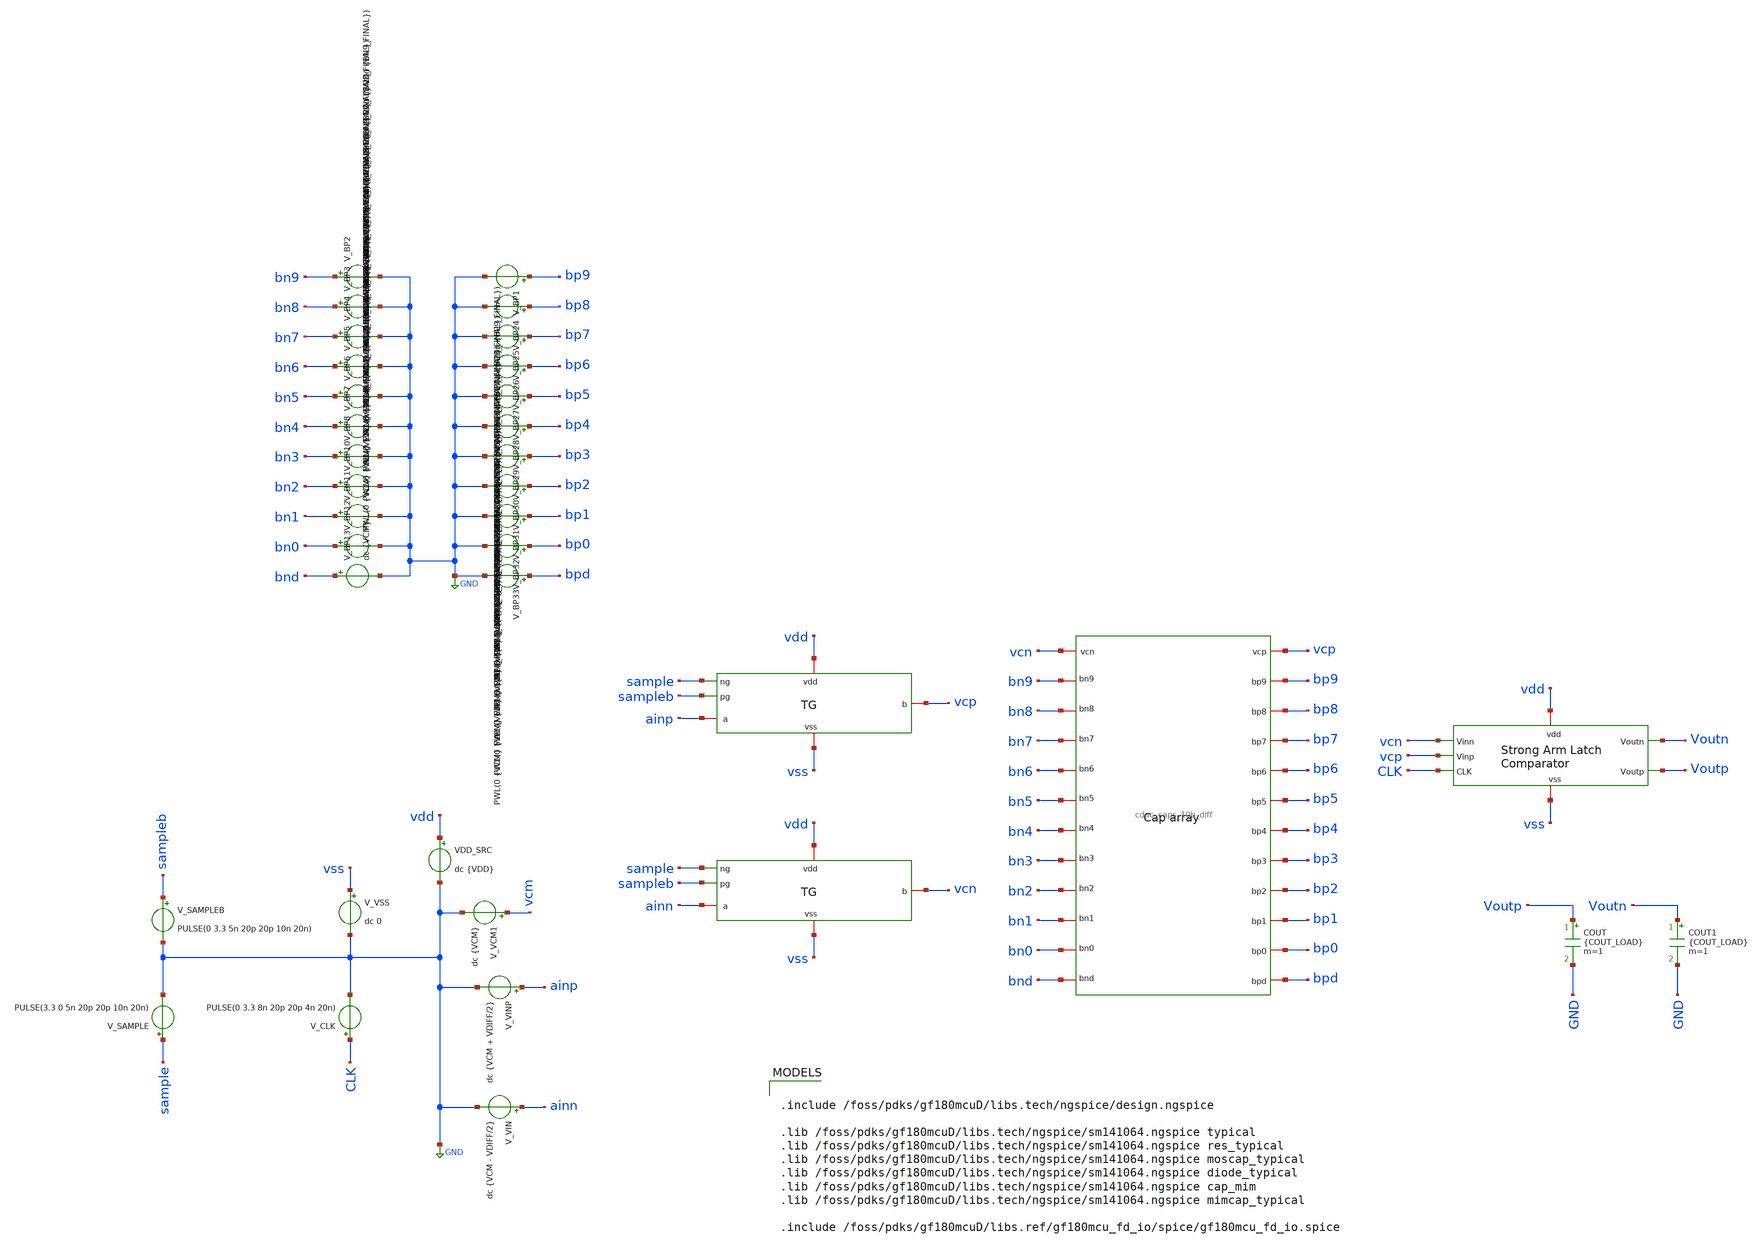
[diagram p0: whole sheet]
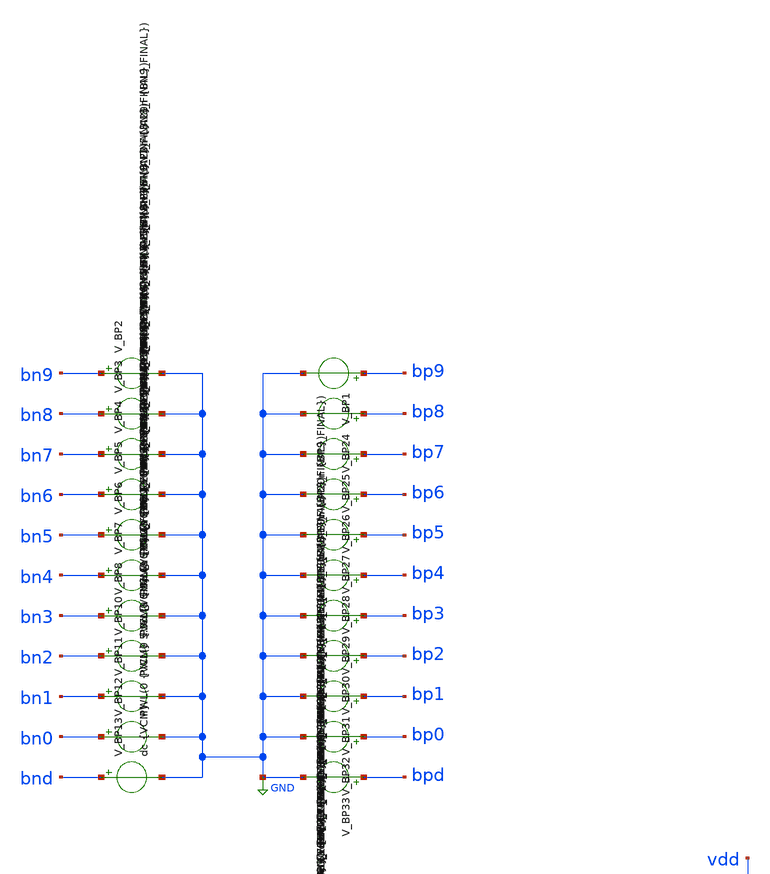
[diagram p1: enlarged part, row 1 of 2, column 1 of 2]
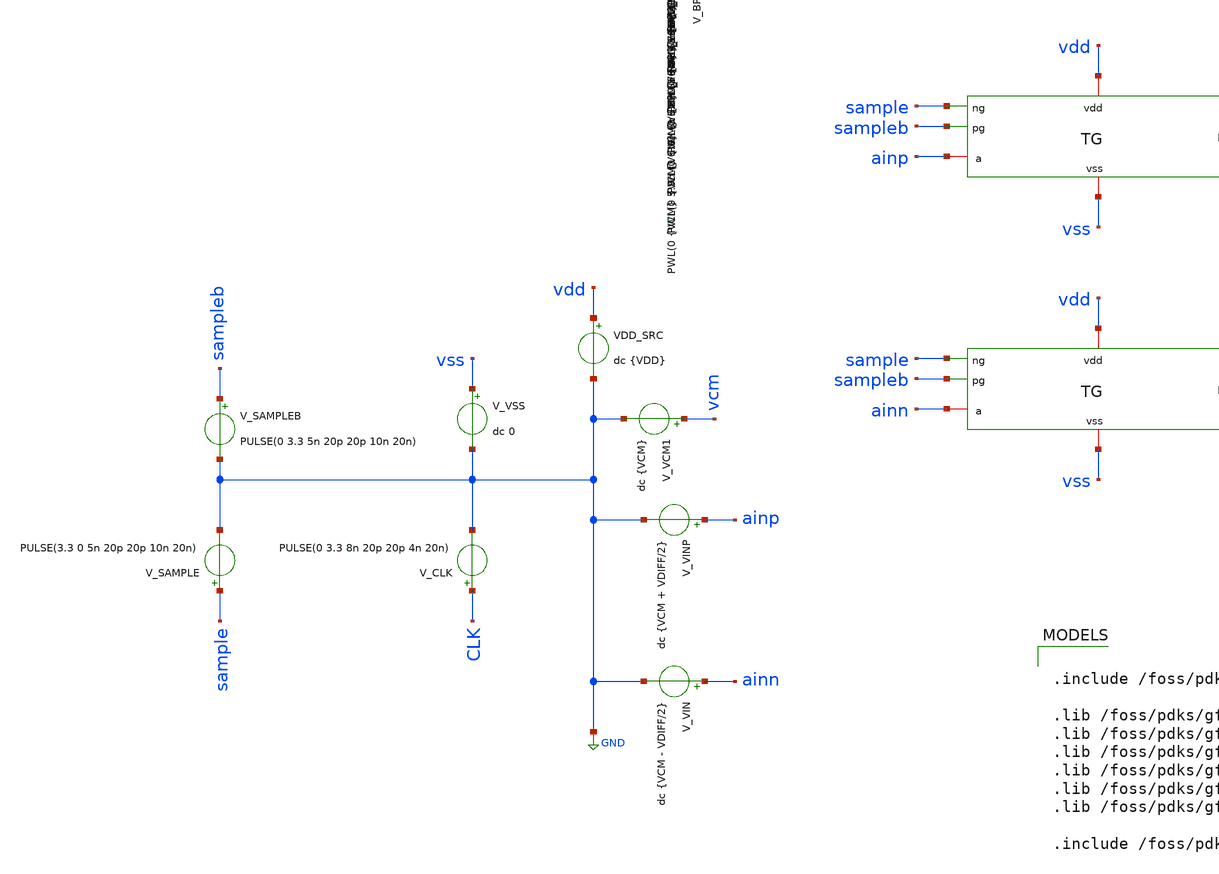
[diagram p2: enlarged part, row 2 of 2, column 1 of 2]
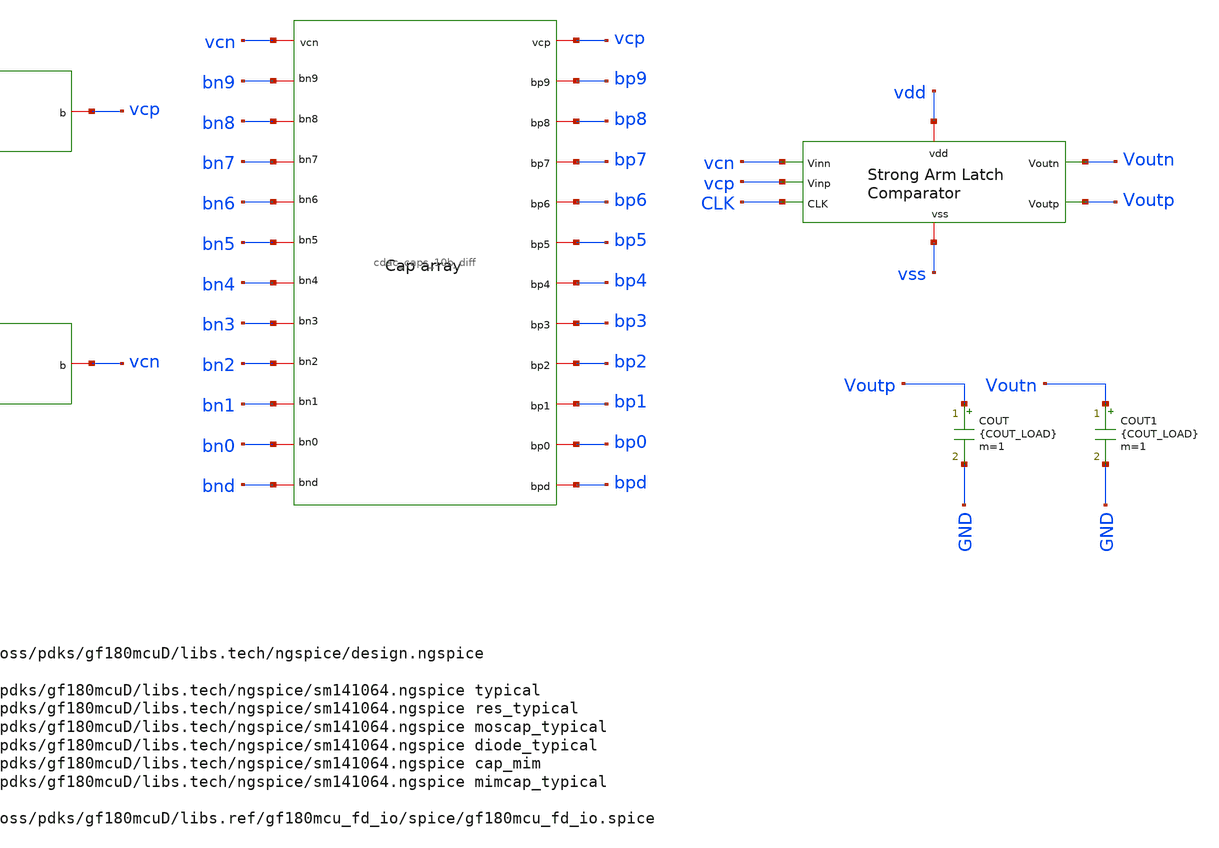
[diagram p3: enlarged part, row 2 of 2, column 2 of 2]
** sch_path: circuit_files/sar_adc_test/tb/cdac_comp_msb_step_tb.sch
**.subckt cdac_comp_msb_step_tb
V_VIN ainn GND dc {VCM - VDIFF/2}
VDD_SRC vdd GND dc {VDD}
V_VINP ainp GND dc {VCM + VDIFF/2}
V_VSS vss GND dc 0
V_CLK CLK GND PULSE(0 3.3 8n 20p 20p 4n 20n)
COUT Voutp GND {COUT_LOAD} m=1
COUT1 Voutn GND {COUT_LOAD} m=1
x1 Voutn vcn Voutp vcp vdd vss CLK strong_arm_comp
x3 vss sample sampleb vdd ainp vcp tg
x4 vss sample sampleb vdd ainn vcn tg
V_SAMPLE sample GND PULSE(3.3 0 5n 20p 20p 10n 20n)
V_SAMPLEB sampleb GND PULSE(0 3.3 5n 20p 20p 10n 20n)
V_VCM1 vcm GND dc {VCM}
x2 vcp bp3 bp0 bp5 bp2 bpd bp1 bp7 bp6 bp8 bp4 bp9 vcn bn0 bn1 bn8 bn7 bn6 bn5 bn4 bn3 bn9 bn2 bnd
+ cdac_caps_10b_diff
V_BP1 bp9 GND PWL(0 {VCM} 5.9n {VCM} 6n {BP9_FINAL} 20n {BP9_FINAL})
V_BP24 bp8 GND PWL(0 {VCM} 5.9n {VCM} 6n {BP8_FINAL} 20n {BP8_FINAL})
V_BP25 bp7 GND PWL(0 {VCM} 5.9n {VCM} 6n {BP7_FINAL} 20n {BP7_FINAL})
V_BP26 bp6 GND PWL(0 {VCM} 5.9n {VCM} 6n {BP6_FINAL} 20n {BP6_FINAL})
V_BP27 bp5 GND PWL(0 {VCM} 5.9n {VCM} 6n {BP5_FINAL} 20n {BP5_FINAL})
V_BP28 bp4 GND PWL(0 {VCM} 5.9n {VCM} 6n {BP4_FINAL} 20n {BP4_FINAL})
V_BP29 bp3 GND PWL(0 {VCM} 5.9n {VCM} 6n {BP3_FINAL} 20n {BP3_FINAL})
V_BP30 bp2 GND PWL(0 {VCM} 5.9n {VCM} 6n {BP2_FINAL} 20n {BP2_FINAL})
V_BP31 bp1 GND PWL(0 {VCM} 5.9n {VCM} 6n {BP1_FINAL} 20n {BP1_FINAL})
V_BP32 bp0 GND PWL(0 {VCM} 5.9n {VCM} 6n {BP0_FINAL} 20n {BP0_FINAL})
V_BP33 bpd GND dc {VCM}
V_BP2 bn9 GND PWL(0 {VCM} 5.9n {VCM} 6n {BN9_FINAL} 20n {BN9_FINAL})
V_BP3 bn8 GND PWL(0 {VCM} 5.9n {VCM} 6n {BN8_FINAL} 20n {BN8_FINAL})
V_BP4 bn7 GND PWL(0 {VCM} 5.9n {VCM} 6n {BN7_FINAL} 20n {BN7_FINAL})
V_BP5 bn6 GND PWL(0 {VCM} 5.9n {VCM} 6n {BN6_FINAL} 20n {BN6_FINAL})
V_BP6 bn5 GND PWL(0 {VCM} 5.9n {VCM} 6n {BN5_FINAL} 20n {BN5_FINAL})
V_BP7 bn4 GND PWL(0 {VCM} 5.9n {VCM} 6n {BN4_FINAL} 20n {BN4_FINAL})
V_BP8 bn3 GND PWL(0 {VCM} 5.9n {VCM} 6n {BN3_FINAL} 20n {BN3_FINAL})
V_BP10 bn2 GND PWL(0 {VCM} 5.9n {VCM} 6n {BN2_FINAL} 20n {BN2_FINAL})
V_BP11 bn1 GND PWL(0 {VCM} 5.9n {VCM} 6n {BN1_FINAL} 20n {BN1_FINAL})
V_BP12 bn0 GND PWL(0 {VCM} 5.9n {VCM} 6n {BN0_FINAL} 20n {BN0_FINAL})
V_BP13 bnd GND dc {VCM}
**** begin user architecture code

.include /foss/pdks/gf180mcuD/libs.tech/ngspice/design.ngspice

.lib /foss/pdks/gf180mcuD/libs.tech/ngspice/sm141064.ngspice typical
.lib /foss/pdks/gf180mcuD/libs.tech/ngspice/sm141064.ngspice res_typical
.lib /foss/pdks/gf180mcuD/libs.tech/ngspice/sm141064.ngspice moscap_typical
.lib /foss/pdks/gf180mcuD/libs.tech/ngspice/sm141064.ngspice diode_typical
.lib /foss/pdks/gf180mcuD/libs.tech/ngspice/sm141064.ngspice cap_mim
.lib /foss/pdks/gf180mcuD/libs.tech/ngspice/sm141064.ngspice mimcap_typical

.include /foss/pdks/gf180mcuD/libs.ref/gf180mcu_fd_io/spice/gf180mcu_fd_io.spice



.param VDD=3.3
.param VCM=1.65
.param VDIFF=0
.param WCU=5u
.param LCU=5u
.param COUT_LOAD=20f

* Positive MSB test:
* bp9 goes high, bn9 goes low.
.param BP9_FINAL={VDD}
.param BN9_FINAL=0

* All other bits stay at VCM.
.param BP8_FINAL={VCM}
.param BP7_FINAL={VCM}
.param BP6_FINAL={VCM}
.param BP5_FINAL={VCM}
.param BP4_FINAL={VCM}
.param BP3_FINAL={VCM}
.param BP2_FINAL={VCM}
.param BP1_FINAL={VCM}
.param BP0_FINAL={VCM}

.param BN8_FINAL={VCM}
.param BN7_FINAL={VCM}
.param BN6_FINAL={VCM}
.param BN5_FINAL={VCM}
.param BN4_FINAL={VCM}
.param BN3_FINAL={VCM}
.param BN2_FINAL={VCM}
.param BN1_FINAL={VCM}
.param BN0_FINAL={VCM}


.options savecurrents
.options reltol=1e-4 abstol=1e-12 vntol=1e-6 method=gear

.save v(sample) v(sampleb) v(CLK)
.save v(ainp) v(ainn)
.save v(vcp) v(vcn)
.save v(bp9) v(bn9)
.save v(Voutp) v(Voutn)
.save i(VDD_SRC)

.control

shell rm -f cdac_bit_weight_sweep_results.txt

echo ================================================== > cdac_bit_weight_sweep_results.txt
echo CDAC BIT-WEIGHT SWEEP RESULTS >> cdac_bit_weight_sweep_results.txt
echo ================================================== >> cdac_bit_weight_sweep_results.txt
echo Sweep type: positive differential CDAC steps >> cdac_bit_weight_sweep_results.txt
echo For each bit k: bp[k] switches VCM to VDD, bn[k] switches VCM to 0 >>
+ cdac_bit_weight_sweep_results.txt
echo All other bottom plates stay at VCM >> cdac_bit_weight_sweep_results.txt
echo Dummy caps bpd and bnd stay at VCM >> cdac_bit_weight_sweep_results.txt
echo VDD = 3.3 V >> cdac_bit_weight_sweep_results.txt
echo VCM = 1.65 V >> cdac_bit_weight_sweep_results.txt
echo Unit cap uses cap_mim_2f0fF with WCU=5um and LCU=5um >> cdac_bit_weight_sweep_results.txt
echo Approx Cu = 2 fF/um2 * 5um * 5um = 50 fF >> cdac_bit_weight_sweep_results.txt
echo Approx total capacitance per side = 1024*50fF = 51.2 pF >> cdac_bit_weight_sweep_results.txt
echo Sample turns OFF at 5 ns >> cdac_bit_weight_sweep_results.txt
echo CDAC bottom plates switch at 6 ns >> cdac_bit_weight_sweep_results.txt
echo CDAC step measured at 7 ns >> cdac_bit_weight_sweep_results.txt
echo Comparator CLK rises at 8 ns >> cdac_bit_weight_sweep_results.txt
echo Comparator output measured at 10 ns >> cdac_bit_weight_sweep_results.txt
echo pass_weight = 1 if CDAC step error is less than 10 percent >> cdac_bit_weight_sweep_results.txt
echo pass_comp = 1 if comparator output has correct positive polarity >>
+ cdac_bit_weight_sweep_results.txt
echo ================================================== >> cdac_bit_weight_sweep_results.txt
echo columns: BIT expected_step measured_step abs_error rel_error_percent vdiff_before vdiff_after
+ vcp_5p5 vcn_5p5 vcp_7 vcn_7 cm_7 voutp_10 voutn_10 outdiff_10 pass_weight pass_comp iavg_0_10ns pavg_0_10ns
+ >> cdac_bit_weight_sweep_results.txt
echo ================================================== >> cdac_bit_weight_sweep_results.txt


* ==================================================
* BIT 9 POSITIVE STEP
* ==================================================
alterparam BP9_FINAL = 3.3
alterparam BP8_FINAL = 1.65
alterparam BP7_FINAL = 1.65
alterparam BP6_FINAL = 1.65
alterparam BP5_FINAL = 1.65
alterparam BP4_FINAL = 1.65
alterparam BP3_FINAL = 1.65
alterparam BP2_FINAL = 1.65
alterparam BP1_FINAL = 1.65
alterparam BP0_FINAL = 1.65

alterparam BN9_FINAL = 0
alterparam BN8_FINAL = 1.65
alterparam BN7_FINAL = 1.65
alterparam BN6_FINAL = 1.65
alterparam BN5_FINAL = 1.65
alterparam BN4_FINAL = 1.65
alterparam BN3_FINAL = 1.65
alterparam BN2_FINAL = 1.65
alterparam BN1_FINAL = 1.65
alterparam BN0_FINAL = 1.65

reset
tran 1p 12n

meas tran vcp55 FIND v(vcp) AT=5.5n
meas tran vcn55 FIND v(vcn) AT=5.5n
let vdiff_before = vcp55 - vcn55

meas tran vcp7 FIND v(vcp) AT=7n
meas tran vcn7 FIND v(vcn) AT=7n
let vdiff_after = vcp7 - vcn7
let measured_step = vdiff_after - vdiff_before
let expected_step = 1.65
let abs_error = abs(measured_step - expected_step)
let rel_error_percent = 100*abs_error/expected_step
let cm7 = 0.5*(vcp7 + vcn7)

meas tran voutp10 FIND v(Voutp) AT=10n
meas tran voutn10 FIND v(Voutn) AT=10n
let outdiff10 = voutp10 - voutn10

let pass_weight = 0
if rel_error_percent < 10
  let pass_weight = 1
end

let pass_comp = 0
if outdiff10 > 2.5
  let pass_comp = 1
end

meas tran iavg AVG i(VDD_SRC) FROM=0n TO=10n
let pavg = abs(3.3*iavg)

echo 9 $&expected_step $&measured_step $&abs_error $&rel_error_percent $&vdiff_before $&vdiff_after
+ $&vcp55 $&vcn55 $&vcp7 $&vcn7 $&cm7 $&voutp10 $&voutn10 $&outdiff10 $&pass_weight $&pass_comp $&iavg $&pavg
+ >> cdac_bit_weight_sweep_results.txt


* ==================================================
* BIT 8 POSITIVE STEP
* ==================================================
alterparam BP9_FINAL = 1.65
alterparam BP8_FINAL = 3.3
alterparam BP7_FINAL = 1.65
alterparam BP6_FINAL = 1.65
alterparam BP5_FINAL = 1.65
alterparam BP4_FINAL = 1.65
alterparam BP3_FINAL = 1.65
alterparam BP2_FINAL = 1.65
alterparam BP1_FINAL = 1.65
alterparam BP0_FINAL = 1.65

alterparam BN9_FINAL = 1.65
alterparam BN8_FINAL = 0
alterparam BN7_FINAL = 1.65
alterparam BN6_FINAL = 1.65
alterparam BN5_FINAL = 1.65
alterparam BN4_FINAL = 1.65
alterparam BN3_FINAL = 1.65
alterparam BN2_FINAL = 1.65
alterparam BN1_FINAL = 1.65
alterparam BN0_FINAL = 1.65

reset
tran 1p 12n

meas tran vcp55 FIND v(vcp) AT=5.5n
meas tran vcn55 FIND v(vcn) AT=5.5n
let vdiff_before = vcp55 - vcn55

meas tran vcp7 FIND v(vcp) AT=7n
meas tran vcn7 FIND v(vcn) AT=7n
let vdiff_after = vcp7 - vcn7
let measured_step = vdiff_after - vdiff_before
let expected_step = 0.825
let abs_error = abs(measured_step - expected_step)
let rel_error_percent = 100*abs_error/expected_step
let cm7 = 0.5*(vcp7 + vcn7)

meas tran voutp10 FIND v(Voutp) AT=10n
meas tran voutn10 FIND v(Voutn) AT=10n
let outdiff10 = voutp10 - voutn10

let pass_weight = 0
if rel_error_percent < 10
  let pass_weight = 1
end

let pass_comp = 0
if outdiff10 > 2.5
  let pass_comp = 1
end

meas tran iavg AVG i(VDD_SRC) FROM=0n TO=10n
let pavg = abs(3.3*iavg)

echo 8 $&expected_step $&measured_step $&abs_error $&rel_error_percent $&vdiff_before $&vdiff_after
+ $&vcp55 $&vcn55 $&vcp7 $&vcn7 $&cm7 $&voutp10 $&voutn10 $&outdiff10 $&pass_weight $&pass_comp $&iavg $&pavg
+ >> cdac_bit_weight_sweep_results.txt


* ==================================================
* BIT 7 POSITIVE STEP
* ==================================================
alterparam BP9_FINAL = 1.65
alterparam BP8_FINAL = 1.65
alterparam BP7_FINAL = 3.3
alterparam BP6_FINAL = 1.65
alterparam BP5_FINAL = 1.65
alterparam BP4_FINAL = 1.65
alterparam BP3_FINAL = 1.65
alterparam BP2_FINAL = 1.65
alterparam BP1_FINAL = 1.65
alterparam BP0_FINAL = 1.65

alterparam BN9_FINAL = 1.65
alterparam BN8_FINAL = 1.65
alterparam BN7_FINAL = 0
alterparam BN6_FINAL = 1.65
alterparam BN5_FINAL = 1.65
alterparam BN4_FINAL = 1.65
alterparam BN3_FINAL = 1.65
alterparam BN2_FINAL = 1.65
alterparam BN1_FINAL = 1.65
alterparam BN0_FINAL = 1.65

reset
tran 1p 12n

meas tran vcp55 FIND v(vcp) AT=5.5n
meas tran vcn55 FIND v(vcn) AT=5.5n
let vdiff_before = vcp55 - vcn55

meas tran vcp7 FIND v(vcp) AT=7n
meas tran vcn7 FIND v(vcn) AT=7n
let vdiff_after = vcp7 - vcn7
let measured_step = vdiff_after - vdiff_before
let expected_step = 0.4125
let abs_error = abs(measured_step - expected_step)
let rel_error_percent = 100*abs_error/expected_step
let cm7 = 0.5*(vcp7 + vcn7)

meas tran voutp10 FIND v(Voutp) AT=10n
meas tran voutn10 FIND v(Voutn) AT=10n
let outdiff10 = voutp10 - voutn10

let pass_weight = 0
if rel_error_percent < 10
  let pass_weight = 1
end

let pass_comp = 0
if outdiff10 > 2.5
  let pass_comp = 1
end

meas tran iavg AVG i(VDD_SRC) FROM=0n TO=10n
let pavg = abs(3.3*iavg)

echo 7 $&expected_step $&measured_step $&abs_error $&rel_error_percent $&vdiff_before $&vdiff_after
+ $&vcp55 $&vcn55 $&vcp7 $&vcn7 $&cm7 $&voutp10 $&voutn10 $&outdiff10 $&pass_weight $&pass_comp $&iavg $&pavg
+ >> cdac_bit_weight_sweep_results.txt


* ==================================================
* BIT 6 POSITIVE STEP
* ==================================================
alterparam BP9_FINAL = 1.65
alterparam BP8_FINAL = 1.65
alterparam BP7_FINAL = 1.65
alterparam BP6_FINAL = 3.3
alterparam BP5_FINAL = 1.65
alterparam BP4_FINAL = 1.65
alterparam BP3_FINAL = 1.65
alterparam BP2_FINAL = 1.65
alterparam BP1_FINAL = 1.65
alterparam BP0_FINAL = 1.65

alterparam BN9_FINAL = 1.65
alterparam BN8_FINAL = 1.65
alterparam BN7_FINAL = 1.65
alterparam BN6_FINAL = 0
alterparam BN5_FINAL = 1.65
alterparam BN4_FINAL = 1.65
alterparam BN3_FINAL = 1.65
alterparam BN2_FINAL = 1.65
alterparam BN1_FINAL = 1.65
alterparam BN0_FINAL = 1.65

reset
tran 1p 12n

meas tran vcp55 FIND v(vcp) AT=5.5n
meas tran vcn55 FIND v(vcn) AT=5.5n
let vdiff_before = vcp55 - vcn55

meas tran vcp7 FIND v(vcp) AT=7n
meas tran vcn7 FIND v(vcn) AT=7n
let vdiff_after = vcp7 - vcn7
let measured_step = vdiff_after - vdiff_before
let expected_step = 0.20625
let abs_error = abs(measured_step - expected_step)
let rel_error_percent = 100*abs_error/expected_step
let cm7 = 0.5*(vcp7 + vcn7)

meas tran voutp10 FIND v(Voutp) AT=10n
meas tran voutn10 FIND v(Voutn) AT=10n
let outdiff10 = voutp10 - voutn10

let pass_weight = 0
if rel_error_percent < 10
  let pass_weight = 1
end

let pass_comp = 0
if outdiff10 > 2.5
  let pass_comp = 1
end

meas tran iavg AVG i(VDD_SRC) FROM=0n TO=10n
let pavg = abs(3.3*iavg)

echo 6 $&expected_step $&measured_step $&abs_error $&rel_error_percent $&vdiff_before $&vdiff_after
+ $&vcp55 $&vcn55 $&vcp7 $&vcn7 $&cm7 $&voutp10 $&voutn10 $&outdiff10 $&pass_weight $&pass_comp $&iavg $&pavg
+ >> cdac_bit_weight_sweep_results.txt


* ==================================================
* BIT 5 POSITIVE STEP
* ==================================================
alterparam BP9_FINAL = 1.65
alterparam BP8_FINAL = 1.65
alterparam BP7_FINAL = 1.65
alterparam BP6_FINAL = 1.65
alterparam BP5_FINAL = 3.3
alterparam BP4_FINAL = 1.65
alterparam BP3_FINAL = 1.65
alterparam BP2_FINAL = 1.65
alterparam BP1_FINAL = 1.65
alterparam BP0_FINAL = 1.65

alterparam BN9_FINAL = 1.65
alterparam BN8_FINAL = 1.65
alterparam BN7_FINAL = 1.65
alterparam BN6_FINAL = 1.65
alterparam BN5_FINAL = 0
alterparam BN4_FINAL = 1.65
alterparam BN3_FINAL = 1.65
alterparam BN2_FINAL = 1.65
alterparam BN1_FINAL = 1.65
alterparam BN0_FINAL = 1.65

reset
tran 1p 12n

meas tran vcp55 FIND v(vcp) AT=5.5n
meas tran vcn55 FIND v(vcn) AT=5.5n
let vdiff_before = vcp55 - vcn55

meas tran vcp7 FIND v(vcp) AT=7n
meas tran vcn7 FIND v(vcn) AT=7n
let vdiff_after = vcp7 - vcn7
let measured_step = vdiff_after - vdiff_before
let expected_step = 0.103125
let abs_error = abs(measured_step - expected_step)
let rel_error_percent = 100*abs_error/expected_step
let cm7 = 0.5*(vcp7 + vcn7)

meas tran voutp10 FIND v(Voutp) AT=10n
meas tran voutn10 FIND v(Voutn) AT=10n
let outdiff10 = voutp10 - voutn10

let pass_weight = 0
if rel_error_percent < 10
  let pass_weight = 1
end

let pass_comp = 0
if outdiff10 > 2.5
  let pass_comp = 1
end

meas tran iavg AVG i(VDD_SRC) FROM=0n TO=10n
let pavg = abs(3.3*iavg)

echo 5 $&expected_step $&measured_step $&abs_error $&rel_error_percent $&vdiff_before $&vdiff_after
+ $&vcp55 $&vcn55 $&vcp7 $&vcn7 $&cm7 $&voutp10 $&voutn10 $&outdiff10 $&pass_weight $&pass_comp $&iavg $&pavg
+ >> cdac_bit_weight_sweep_results.txt


* ==================================================
* BIT 4 POSITIVE STEP
* ==================================================
alterparam BP9_FINAL = 1.65
alterparam BP8_FINAL = 1.65
alterparam BP7_FINAL = 1.65
alterparam BP6_FINAL = 1.65
alterparam BP5_FINAL = 1.65
alterparam BP4_FINAL = 3.3
alterparam BP3_FINAL = 1.65
alterparam BP2_FINAL = 1.65
alterparam BP1_FINAL = 1.65
alterparam BP0_FINAL = 1.65

alterparam BN9_FINAL = 1.65
alterparam BN8_FINAL = 1.65
alterparam BN7_FINAL = 1.65
alterparam BN6_FINAL = 1.65
alterparam BN5_FINAL = 1.65
alterparam BN4_FINAL = 0
alterparam BN3_FINAL = 1.65
alterparam BN2_FINAL = 1.65
alterparam BN1_FINAL = 1.65
alterparam BN0_FINAL = 1.65

reset
tran 1p 12n

meas tran vcp55 FIND v(vcp) AT=5.5n
meas tran vcn55 FIND v(vcn) AT=5.5n
let vdiff_before = vcp55 - vcn55

meas tran vcp7 FIND v(vcp) AT=7n
meas tran vcn7 FIND v(vcn) AT=7n
let vdiff_after = vcp7 - vcn7
let measured_step = vdiff_after - vdiff_before
let expected_step = 0.0515625
let abs_error = abs(measured_step - expected_step)
let rel_error_percent = 100*abs_error/expected_step
let cm7 = 0.5*(vcp7 + vcn7)

meas tran voutp10 FIND v(Voutp) AT=10n
meas tran voutn10 FIND v(Voutn) AT=10n
let outdiff10 = voutp10 - voutn10

let pass_weight = 0
if rel_error_percent < 10
  let pass_weight = 1
end

let pass_comp = 0
if outdiff10 > 2.5
  let pass_comp = 1
end

meas tran iavg AVG i(VDD_SRC) FROM=0n TO=10n
let pavg = abs(3.3*iavg)

echo 4 $&expected_step $&measured_step $&abs_error $&rel_error_percent $&vdiff_before $&vdiff_after
+ $&vcp55 $&vcn55 $&vcp7 $&vcn7 $&cm7 $&voutp10 $&voutn10 $&outdiff10 $&pass_weight $&pass_comp $&iavg $&pavg
+ >> cdac_bit_weight_sweep_results.txt


* ==================================================
* BIT 3 POSITIVE STEP
* ==================================================
alterparam BP9_FINAL = 1.65
alterparam BP8_FINAL = 1.65
alterparam BP7_FINAL = 1.65
alterparam BP6_FINAL = 1.65
alterparam BP5_FINAL = 1.65
alterparam BP4_FINAL = 1.65
alterparam BP3_FINAL = 3.3
alterparam BP2_FINAL = 1.65
alterparam BP1_FINAL = 1.65
alterparam BP0_FINAL = 1.65

alterparam BN9_FINAL = 1.65
alterparam BN8_FINAL = 1.65
alterparam BN7_FINAL = 1.65
alterparam BN6_FINAL = 1.65
alterparam BN5_FINAL = 1.65
alterparam BN4_FINAL = 1.65
alterparam BN3_FINAL = 0
alterparam BN2_FINAL = 1.65
alterparam BN1_FINAL = 1.65
alterparam BN0_FINAL = 1.65

reset
tran 1p 12n

meas tran vcp55 FIND v(vcp) AT=5.5n
meas tran vcn55 FIND v(vcn) AT=5.5n
let vdiff_before = vcp55 - vcn55

meas tran vcp7 FIND v(vcp) AT=7n
meas tran vcn7 FIND v(vcn) AT=7n
let vdiff_after = vcp7 - vcn7
let measured_step = vdiff_after - vdiff_before
let expected_step = 0.02578125
let abs_error = abs(measured_step - expected_step)
let rel_error_percent = 100*abs_error/expected_step
let cm7 = 0.5*(vcp7 + vcn7)

meas tran voutp10 FIND v(Voutp) AT=10n
meas tran voutn10 FIND v(Voutn) AT=10n
let outdiff10 = voutp10 - voutn10

let pass_weight = 0
if rel_error_percent < 10
  let pass_weight = 1
end

let pass_comp = 0
if outdiff10 > 2.5
  let pass_comp = 1
end

meas tran iavg AVG i(VDD_SRC) FROM=0n TO=10n
let pavg = abs(3.3*iavg)

echo 3 $&expected_step $&measured_step $&abs_error $&rel_error_percent $&vdiff_before $&vdiff_after
+ $&vcp55 $&vcn55 $&vcp7 $&vcn7 $&cm7 $&voutp10 $&voutn10 $&outdiff10 $&pass_weight $&pass_comp $&iavg $&pavg
+ >> cdac_bit_weight_sweep_results.txt


* ==================================================
* BIT 2 POSITIVE STEP
* ==================================================
alterparam BP9_FINAL = 1.65
alterparam BP8_FINAL = 1.65
alterparam BP7_FINAL = 1.65
alterparam BP6_FINAL = 1.65
alterparam BP5_FINAL = 1.65
alterparam BP4_FINAL = 1.65
alterparam BP3_FINAL = 1.65
alterparam BP2_FINAL = 3.3
alterparam BP1_FINAL = 1.65
alterparam BP0_FINAL = 1.65

alterparam BN9_FINAL = 1.65
alterparam BN8_FINAL = 1.65
alterparam BN7_FINAL = 1.65
alterparam BN6_FINAL = 1.65
alterparam BN5_FINAL = 1.65
alterparam BN4_FINAL = 1.65
alterparam BN3_FINAL = 1.65
alterparam BN2_FINAL = 0
alterparam BN1_FINAL = 1.65
alterparam BN0_FINAL = 1.65

reset
tran 1p 12n

meas tran vcp55 FIND v(vcp) AT=5.5n
meas tran vcn55 FIND v(vcn) AT=5.5n
let vdiff_before = vcp55 - vcn55

meas tran vcp7 FIND v(vcp) AT=7n
meas tran vcn7 FIND v(vcn) AT=7n
let vdiff_after = vcp7 - vcn7
let measured_step = vdiff_after - vdiff_before
let expected_step = 0.012890625
let abs_error = abs(measured_step - expected_step)
let rel_error_percent = 100*abs_error/expected_step
let cm7 = 0.5*(vcp7 + vcn7)

meas tran voutp10 FIND v(Voutp) AT=10n
meas tran voutn10 FIND v(Voutn) AT=10n
let outdiff10 = voutp10 - voutn10

let pass_weight = 0
if rel_error_percent < 10
  let pass_weight = 1
end

let pass_comp = 0
if outdiff10 > 2.5
  let pass_comp = 1
end

meas tran iavg AVG i(VDD_SRC) FROM=0n TO=10n
let pavg = abs(3.3*iavg)

echo 2 $&expected_step $&measured_step $&abs_error $&rel_error_percent $&vdiff_before $&vdiff_after
+ $&vcp55 $&vcn55 $&vcp7 $&vcn7 $&cm7 $&voutp10 $&voutn10 $&outdiff10 $&pass_weight $&pass_comp $&iavg $&pavg
+ >> cdac_bit_weight_sweep_results.txt


* ==================================================
* BIT 1 POSITIVE STEP
* ==================================================
alterparam BP9_FINAL = 1.65
alterparam BP8_FINAL = 1.65
alterparam BP7_FINAL = 1.65
alterparam BP6_FINAL = 1.65
alterparam BP5_FINAL = 1.65
alterparam BP4_FINAL = 1.65
alterparam BP3_FINAL = 1.65
alterparam BP2_FINAL = 1.65
alterparam BP1_FINAL = 3.3
alterparam BP0_FINAL = 1.65

alterparam BN9_FINAL = 1.65
alterparam BN8_FINAL = 1.65
alterparam BN7_FINAL = 1.65
alterparam BN6_FINAL = 1.65
alterparam BN5_FINAL = 1.65
alterparam BN4_FINAL = 1.65
alterparam BN3_FINAL = 1.65
alterparam BN2_FINAL = 1.65
alterparam BN1_FINAL = 0
alterparam BN0_FINAL = 1.65

reset
tran 1p 12n

meas tran vcp55 FIND v(vcp) AT=5.5n
meas tran vcn55 FIND v(vcn) AT=5.5n
let vdiff_before = vcp55 - vcn55

meas tran vcp7 FIND v(vcp) AT=7n
meas tran vcn7 FIND v(vcn) AT=7n
let vdiff_after = vcp7 - vcn7
let measured_step = vdiff_after - vdiff_before
let expected_step = 0.0064453125
let abs_error = abs(measured_step - expected_step)
let rel_error_percent = 100*abs_error/expected_step
let cm7 = 0.5*(vcp7 + vcn7)

meas tran voutp10 FIND v(Voutp) AT=10n
meas tran voutn10 FIND v(Voutn) AT=10n
let outdiff10 = voutp10 - voutn10

let pass_weight = 0
if rel_error_percent < 10
  let pass_weight = 1
end

let pass_comp = 0
if outdiff10 > 2.5
  let pass_comp = 1
end

meas tran iavg AVG i(VDD_SRC) FROM=0n TO=10n
let pavg = abs(3.3*iavg)

echo 1 $&expected_step $&measured_step $&abs_error $&rel_error_percent $&vdiff_before $&vdiff_after
+ $&vcp55 $&vcn55 $&vcp7 $&vcn7 $&cm7 $&voutp10 $&voutn10 $&outdiff10 $&pass_weight $&pass_comp $&iavg $&pavg
+ >> cdac_bit_weight_sweep_results.txt


* ==================================================
* BIT 0 POSITIVE STEP
* ==================================================
alterparam BP9_FINAL = 1.65
alterparam BP8_FINAL = 1.65
alterparam BP7_FINAL = 1.65
alterparam BP6_FINAL = 1.65
alterparam BP5_FINAL = 1.65
alterparam BP4_FINAL = 1.65
alterparam BP3_FINAL = 1.65
alterparam BP2_FINAL = 1.65
alterparam BP1_FINAL = 1.65
alterparam BP0_FINAL = 3.3

alterparam BN9_FINAL = 1.65
alterparam BN8_FINAL = 1.65
alterparam BN7_FINAL = 1.65
alterparam BN6_FINAL = 1.65
alterparam BN5_FINAL = 1.65
alterparam BN4_FINAL = 1.65
alterparam BN3_FINAL = 1.65
alterparam BN2_FINAL = 1.65
alterparam BN1_FINAL = 1.65
alterparam BN0_FINAL = 0

reset
tran 1p 12n

meas tran vcp55 FIND v(vcp) AT=5.5n
meas tran vcn55 FIND v(vcn) AT=5.5n
let vdiff_before = vcp55 - vcn55

meas tran vcp7 FIND v(vcp) AT=7n
meas tran vcn7 FIND v(vcn) AT=7n
let vdiff_after = vcp7 - vcn7
let measured_step = vdiff_after - vdiff_before
let expected_step = 0.00322265625
let abs_error = abs(measured_step - expected_step)
let rel_error_percent = 100*abs_error/expected_step
let cm7 = 0.5*(vcp7 + vcn7)

meas tran voutp10 FIND v(Voutp) AT=10n
meas tran voutn10 FIND v(Voutn) AT=10n
let outdiff10 = voutp10 - voutn10

let pass_weight = 0
if rel_error_percent < 10
  let pass_weight = 1
end

let pass_comp = 0
if outdiff10 > 2.5
  let pass_comp = 1
end

meas tran iavg AVG i(VDD_SRC) FROM=0n TO=10n
let pavg = abs(3.3*iavg)

echo 0 $&expected_step $&measured_step $&abs_error $&rel_error_percent $&vdiff_before $&vdiff_after
+ $&vcp55 $&vcn55 $&vcp7 $&vcn7 $&cm7 $&voutp10 $&voutn10 $&outdiff10 $&pass_weight $&pass_comp $&iavg $&pavg
+ >> cdac_bit_weight_sweep_results.txt


echo ================================================== >> cdac_bit_weight_sweep_results.txt
echo END OF CDAC BIT-WEIGHT SWEEP >> cdac_bit_weight_sweep_results.txt
echo Expected ideal positive steps: >> cdac_bit_weight_sweep_results.txt
echo bit9 1.650000000 V >> cdac_bit_weight_sweep_results.txt
echo bit8 0.825000000 V >> cdac_bit_weight_sweep_results.txt
echo bit7 0.412500000 V >> cdac_bit_weight_sweep_results.txt
echo bit6 0.206250000 V >> cdac_bit_weight_sweep_results.txt
echo bit5 0.103125000 V >> cdac_bit_weight_sweep_results.txt
echo bit4 0.051562500 V >> cdac_bit_weight_sweep_results.txt
echo bit3 0.025781250 V >> cdac_bit_weight_sweep_results.txt
echo bit2 0.012890625 V >> cdac_bit_weight_sweep_results.txt
echo bit1 0.0064453125 V >> cdac_bit_weight_sweep_results.txt
echo bit0 0.00322265625 V >> cdac_bit_weight_sweep_results.txt
echo ================================================== >> cdac_bit_weight_sweep_results.txt

echo CDAC bit-weight sweep complete. Open cdac_bit_weight_sweep_results.txt.

* ==================================================
* SMALL-DIFFERENTIAL SAMPLER + COMPARATOR TEST
* PDK MIM CDAC, all bottom plates held at VCM
* ==================================================

echo ================================================== >> cdac_bit_weight_sweep_results.txt
echo SMALL-DIFFERENTIAL SAMPLER + COMPARATOR TEST >> cdac_bit_weight_sweep_results.txt
echo ================================================== >> cdac_bit_weight_sweep_results.txt
echo Purpose: verify TG sampler plus PDK-MIM CDAC plus StrongARM comparator at small input
+ differential >> cdac_bit_weight_sweep_results.txt
echo All CDAC bottom plates stay at VCM, no DAC switching step >> cdac_bit_weight_sweep_results.txt
echo VDIFF positive means ainp greater than ainn, expected Voutp high and Voutn low >>
+ cdac_bit_weight_sweep_results.txt
echo VDIFF negative means ainp less than ainn, expected Voutp low and Voutn high >>
+ cdac_bit_weight_sweep_results.txt
echo Half-LSB differential target = 3.3/2048 = 1.611328125 mV >> cdac_bit_weight_sweep_results.txt
echo sample ON measured at 4.5ns, hold measured at 7ns, comparator output measured at 10ns >>
+ cdac_bit_weight_sweep_results.txt
echo ================================================== >> cdac_bit_weight_sweep_results.txt
echo columns: CASE VDIFF_SET expected_sign sample_4p5 sample_5p5 clk_7 clk_8p5 ainp_4p5 ainn_4p5
+ vcp_4p5 vcn_4p5 track_err_p track_err_n vcp_7 vcn_7 vdiff_hold cm_hold voutp_10 voutn_10 outdiff_10
+ pass_sign iavg_0_10ns pavg_0_10ns >> cdac_bit_weight_sweep_results.txt
echo ================================================== >> cdac_bit_weight_sweep_results.txt


* ==================================================
* SMALL POSITIVE HALF-LSB TEST
* VDIFF = +1.611328125m
* Expected: Voutp high, Voutn low
* ==================================================

alterparam VDIFF = 0.001611328125

alterparam BP9_FINAL = 1.65
alterparam BP8_FINAL = 1.65
alterparam BP7_FINAL = 1.65
alterparam BP6_FINAL = 1.65
alterparam BP5_FINAL = 1.65
alterparam BP4_FINAL = 1.65
alterparam BP3_FINAL = 1.65
alterparam BP2_FINAL = 1.65
alterparam BP1_FINAL = 1.65
alterparam BP0_FINAL = 1.65

alterparam BN9_FINAL = 1.65
alterparam BN8_FINAL = 1.65
alterparam BN7_FINAL = 1.65
alterparam BN6_FINAL = 1.65
alterparam BN5_FINAL = 1.65
alterparam BN4_FINAL = 1.65
alterparam BN3_FINAL = 1.65
alterparam BN2_FINAL = 1.65
alterparam BN1_FINAL = 1.65
alterparam BN0_FINAL = 1.65

reset
tran 1p 12n

meas tran sample45 FIND v(sample) AT=4.5n
meas tran sample55 FIND v(sample) AT=5.5n
meas tran clk7 FIND v(CLK) AT=7n
meas tran clk85 FIND v(CLK) AT=8.5n

meas tran ainp45 FIND v(ainp) AT=4.5n
meas tran ainn45 FIND v(ainn) AT=4.5n
meas tran vcp45 FIND v(vcp) AT=4.5n
meas tran vcn45 FIND v(vcn) AT=4.5n

let track_err_p = vcp45 - ainp45
let track_err_n = vcn45 - ainn45

meas tran vcp7sd FIND v(vcp) AT=7n
meas tran vcn7sd FIND v(vcn) AT=7n

let vdiff_hold = vcp7sd - vcn7sd
let cm_hold = 0.5*(vcp7sd + vcn7sd)

meas tran voutp10sd FIND v(Voutp) AT=10n
meas tran voutn10sd FIND v(Voutn) AT=10n

let outdiff10sd = voutp10sd - voutn10sd

let pass_sign = 0
if outdiff10sd > 2.5
  let pass_sign = 1
end

meas tran iavg_sd AVG i(VDD_SRC) FROM=0n TO=10n
let pavg_sd = abs(3.3*iavg_sd)

echo POS_HALF_LSB 0.001611328125 +1 $&sample45 $&sample55 $&clk7 $&clk85 $&ainp45 $&ainn45 $&vcp45
+ $&vcn45 $&track_err_p $&track_err_n $&vcp7sd $&vcn7sd $&vdiff_hold $&cm_hold $&voutp10sd $&voutn10sd
+ $&outdiff10sd $&pass_sign $&iavg_sd $&pavg_sd >> cdac_bit_weight_sweep_results.txt


* ==================================================
* SMALL NEGATIVE HALF-LSB TEST
* VDIFF = -1.611328125m
* Expected: Voutp low, Voutn high
* ==================================================

alterparam VDIFF = -0.001611328125

alterparam BP9_FINAL = 1.65
alterparam BP8_FINAL = 1.65
alterparam BP7_FINAL = 1.65
alterparam BP6_FINAL = 1.65
alterparam BP5_FINAL = 1.65
alterparam BP4_FINAL = 1.65
alterparam BP3_FINAL = 1.65
alterparam BP2_FINAL = 1.65
alterparam BP1_FINAL = 1.65
alterparam BP0_FINAL = 1.65

alterparam BN9_FINAL = 1.65
alterparam BN8_FINAL = 1.65
alterparam BN7_FINAL = 1.65
alterparam BN6_FINAL = 1.65
alterparam BN5_FINAL = 1.65
alterparam BN4_FINAL = 1.65
alterparam BN3_FINAL = 1.65
alterparam BN2_FINAL = 1.65
alterparam BN1_FINAL = 1.65
alterparam BN0_FINAL = 1.65

reset
tran 1p 12n

meas tran sample45 FIND v(sample) AT=4.5n
meas tran sample55 FIND v(sample) AT=5.5n
meas tran clk7 FIND v(CLK) AT=7n
meas tran clk85 FIND v(CLK) AT=8.5n

meas tran ainp45 FIND v(ainp) AT=4.5n
meas tran ainn45 FIND v(ainn) AT=4.5n
meas tran vcp45 FIND v(vcp) AT=4.5n
meas tran vcn45 FIND v(vcn) AT=4.5n

let track_err_p = vcp45 - ainp45
let track_err_n = vcn45 - ainn45

meas tran vcp7sd FIND v(vcp) AT=7n
meas tran vcn7sd FIND v(vcn) AT=7n

let vdiff_hold = vcp7sd - vcn7sd
let cm_hold = 0.5*(vcp7sd + vcn7sd)

meas tran voutp10sd FIND v(Voutp) AT=10n
meas tran voutn10sd FIND v(Voutn) AT=10n

let outdiff10sd = voutp10sd - voutn10sd

let pass_sign = 0
if outdiff10sd < -2.5
  let pass_sign = 1
end

meas tran iavg_sd AVG i(VDD_SRC) FROM=0n TO=10n
let pavg_sd = abs(3.3*iavg_sd)

echo NEG_HALF_LSB -0.001611328125 -1 $&sample45 $&sample55 $&clk7 $&clk85 $&ainp45 $&ainn45 $&vcp45
+ $&vcn45 $&track_err_p $&track_err_n $&vcp7sd $&vcn7sd $&vdiff_hold $&cm_hold $&voutp10sd $&voutn10sd
+ $&outdiff10sd $&pass_sign $&iavg_sd $&pavg_sd >> cdac_bit_weight_sweep_results.txt


* ==================================================
* ZERO-DIFFERENTIAL OBSERVATION TEST
* Not graded because comparator offset / numerical asymmetry decides
* ==================================================

alterparam VDIFF = 0

alterparam BP9_FINAL = 1.65
alterparam BP8_FINAL = 1.65
alterparam BP7_FINAL = 1.65
alterparam BP6_FINAL = 1.65
alterparam BP5_FINAL = 1.65
alterparam BP4_FINAL = 1.65
alterparam BP3_FINAL = 1.65
alterparam BP2_FINAL = 1.65
alterparam BP1_FINAL = 1.65
alterparam BP0_FINAL = 1.65

alterparam BN9_FINAL = 1.65
alterparam BN8_FINAL = 1.65
alterparam BN7_FINAL = 1.65
alterparam BN6_FINAL = 1.65
alterparam BN5_FINAL = 1.65
alterparam BN4_FINAL = 1.65
alterparam BN3_FINAL = 1.65
alterparam BN2_FINAL = 1.65
alterparam BN1_FINAL = 1.65
alterparam BN0_FINAL = 1.65

reset
tran 1p 12n

meas tran sample45 FIND v(sample) AT=4.5n
meas tran sample55 FIND v(sample) AT=5.5n
meas tran clk7 FIND v(CLK) AT=7n
meas tran clk85 FIND v(CLK) AT=8.5n

meas tran ainp45 FIND v(ainp) AT=4.5n
meas tran ainn45 FIND v(ainn) AT=4.5n
meas tran vcp45 FIND v(vcp) AT=4.5n
meas tran vcn45 FIND v(vcn) AT=4.5n

let track_err_p = vcp45 - ainp45
let track_err_n = vcn45 - ainn45

meas tran vcp7sd FIND v(vcp) AT=7n
meas tran vcn7sd FIND v(vcn) AT=7n

let vdiff_hold = vcp7sd - vcn7sd
let cm_hold = 0.5*(vcp7sd + vcn7sd)

meas tran voutp10sd FIND v(Voutp) AT=10n
meas tran voutn10sd FIND v(Voutn) AT=10n

let outdiff10sd = voutp10sd - voutn10sd

let pass_sign = 9

meas tran iavg_sd AVG i(VDD_SRC) FROM=0n TO=10n
let pavg_sd = abs(3.3*iavg_sd)

echo ZERO 0 0 $&sample45 $&sample55 $&clk7 $&clk85 $&ainp45 $&ainn45 $&vcp45 $&vcn45 $&track_err_p
+ $&track_err_n $&vcp7sd $&vcn7sd $&vdiff_hold $&cm_hold $&voutp10sd $&voutn10sd $&outdiff10sd $&pass_sign
+ $&iavg_sd $&pavg_sd >> cdac_bit_weight_sweep_results.txt

echo ================================================== >> cdac_bit_weight_sweep_results.txt
echo END OF SMALL-DIFFERENTIAL SAMPLER + COMPARATOR TEST >> cdac_bit_weight_sweep_results.txt
echo PASS_SIGN: 1 correct, 0 wrong, 9 zero-diff not graded >> cdac_bit_weight_sweep_results.txt
echo Expected POS_HALF_LSB: vdiff_hold positive, Voutp high, Voutn low >>
+ cdac_bit_weight_sweep_results.txt
echo Expected NEG_HALF_LSB: vdiff_hold negative, Voutp low, Voutn high >>
+ cdac_bit_weight_sweep_results.txt
echo ZERO is observation only >> cdac_bit_weight_sweep_results.txt
echo ================================================== >> cdac_bit_weight_sweep_results.txt

.endc



**** end user architecture code
**.ends

* expanding   symbol:  strong_arm_comp.sym # of pins=7
** sym_path: circuit_files/sar_adc_test/xschem/strong_arm_comp.sym
** sch_path: circuit_files/sar_adc_test/xschem/strong_arm_comp.sch
.subckt strong_arm_comp Voutn Vinn Voutp Vinp vdd vss CLK
*.ipin Vinn
*.opin Voutp
*.iopin vdd
*.ipin Vinp
*.ipin CLK
*.iopin vss
*.opin Voutn
XM1 P CLK vdd vdd sg13_hv_pmos w=2u l=0.4u ng=1 m=4 mm_ok=1
XM2 net1 CLK vss vss sg13_hv_nmos w=2u l=0.45u ng=1 m=8 mm_ok=1
XM3 X CLK vdd vdd sg13_hv_pmos w=2u l=0.4u ng=1 m=4 mm_ok=1
XM4 P Vinn net1 vss sg13_hv_nmos w=2u l=0.45u ng=1 m=6 mm_ok=1
XM5 Q Vinp net1 vss sg13_hv_nmos w=2u l=0.45u ng=1 m=6 mm_ok=1
XM6 X Y P vss sg13_hv_nmos w=2u l=0.45u ng=1 m=2 mm_ok=1
XM7 Y X Q vss sg13_hv_nmos w=2u l=0.45u ng=1 m=2 mm_ok=1
XM8 X Y vdd vdd sg13_hv_pmos w=2u l=0.4u ng=1 m=4 mm_ok=1
XM9 Y CLK vdd vdd sg13_hv_pmos w=2u l=0.4u ng=1 m=4 mm_ok=1
XM10 Q CLK vdd vdd sg13_hv_pmos w=2u l=0.4u ng=1 m=4 mm_ok=1
XM11 Y X vdd vdd sg13_hv_pmos w=2u l=0.4u ng=1 m=4 mm_ok=1
XM12 net2 X vss vss sg13_hv_nmos w=2u l=0.45u ng=1 m=1 mm_ok=1
XM13 Voutp net2 vss vss sg13_hv_nmos w=2u l=0.45u ng=1 m=2 mm_ok=1
XM14 Voutn net3 vss vss sg13_hv_nmos w=2u l=0.45u ng=1 m=2 mm_ok=1
XM15 net3 Y vss vss sg13_hv_nmos w=2u l=0.45u ng=1 m=1 mm_ok=1
XM16 net2 X vdd vdd sg13_hv_pmos w=2u l=0.4u ng=1 m=2 mm_ok=1
XM17 Voutp Voutn vdd vdd sg13_hv_pmos w=2u l=0.4u ng=1 m=4 mm_ok=1
XM18 net3 Y vdd vdd sg13_hv_pmos w=2u l=0.4u ng=1 m=2 mm_ok=1
XM19 Voutn Voutp vdd vdd sg13_hv_pmos w=2u l=0.4u ng=1 m=4 mm_ok=1
.ends


* expanding   symbol:  tg.sym # of pins=6
** sym_path: circuit_files/sar_adc_test/xschem/tg.sym
** sch_path: circuit_files/sar_adc_test/xschem/tg.sch
.subckt tg vss ng pg vdd a b
*.ipin ng
*.iopin vdd
*.ipin pg
*.iopin a
*.iopin b
*.iopin vss
XM12 b ng a vss sg13_hv_nmos w=2u l=0.45u ng=1 m=1 mm_ok=1
XM16 b pg a vdd sg13_hv_pmos w=2u l=0.4u ng=1 m=2 mm_ok=1
.ends


* expanding   symbol:  cdac_caps_10b_diff.sym # of pins=24
** sym_path: circuit_files/sar_adc_test/xschem/cdac_caps_10b_diff.sym
** sch_path: circuit_files/sar_adc_test/xschem/cdac_caps_10b_diff.sch
.subckt cdac_caps_10b_diff vcp bp3 bp0 bp5 bp2 bpd bp1 bp7 bp6 bp8 bp4 bp9 vcn bn0 bn1 bn8 bn7 bn6
+ bn5 bn4 bn3 bn9 bn2 bnd
*.iopin vcp
*.iopin vcn
*.iopin bpd
*.iopin bp0
*.iopin bp1
*.iopin bp2
*.iopin bp3
*.iopin bp4
*.iopin bp5
*.iopin bp6
*.iopin bp7
*.iopin bp8
*.iopin bp9
*.iopin bnd
*.iopin bn1
*.iopin bn2
*.iopin bn3
*.iopin bn4
*.iopin bn5
*.iopin bn6
*.iopin bn7
*.iopin bn8
*.iopin bn9
*.iopin bn0
C2 vcp bp0 {1*Cu} m=1
C1 vcp bpd {1*Cu} m=1
C3 vcp bp2 {4*Cu} m=1
C4 vcp bp1 {2*Cu} m=1
C5 vcp bp5 {32*Cu} m=1
C6 vcp bp4 {16*Cu} m=1
C7 vcp bp7 {128*Cu} m=1
C8 vcp bp6 {64*Cu} m=1
C9 vcp bp8 {256*Cu} m=1
C10 vcp bp3 {8*Cu} m=1
C12 vcp bp9 {512*Cu} m=1
C11 vcn bn0 {1*Cu} m=1
C13 vcn bnd {1*Cu} m=1
C14 vcn bn2 {4*Cu} m=1
C15 vcn bn1 {2*Cu} m=1
C16 vcn bn5 {32*Cu} m=1
C17 vcn bn4 {16*Cu} m=1
C18 vcn bn7 {128*Cu} m=1
C19 vcn bn6 {64*Cu} m=1
C20 vcn bn8 {256*Cu} m=1
C21 vcn bn3 {8*Cu} m=1
C22 vcn bn9 {512*Cu} m=1
.ends

.GLOBAL GND
.end
